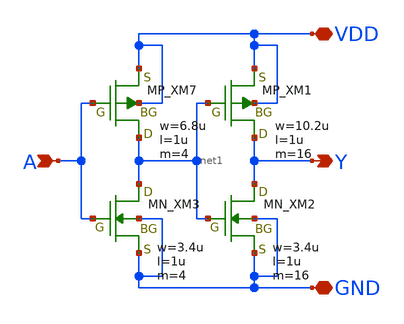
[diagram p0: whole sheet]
** sch_path: openIP62_rev1.0/IP62/Technology/tech/symbols/Xschem/IP62_5_stdcell/BUF_X16.sch
**.subckt BUF_X16 A Y VDD GND
*.ipin A
*.opin Y
*.iopin VDD
*.iopin GND
XM7 net1 A VDD VDD PMOS w=6.8u l=1u as=0 ad=0 ps=0 pd=0 nrd=0 nrs=0 m=4
XM1 Y net1 VDD VDD PMOS w=10.2u l=1u as=0 ad=0 ps=0 pd=0 nrd=0 nrs=0 m=16
XM3 net1 A GND GND NMOS w=3.4u l=1u as=0 ad=0 ps=0 pd=0 nrd=0 nrs=0 m=4
XM2 Y net1 GND GND NMOS w=3.4u l=1u as=0 ad=0 ps=0 pd=0 nrd=0 nrs=0 m=16
**.ends
.end
